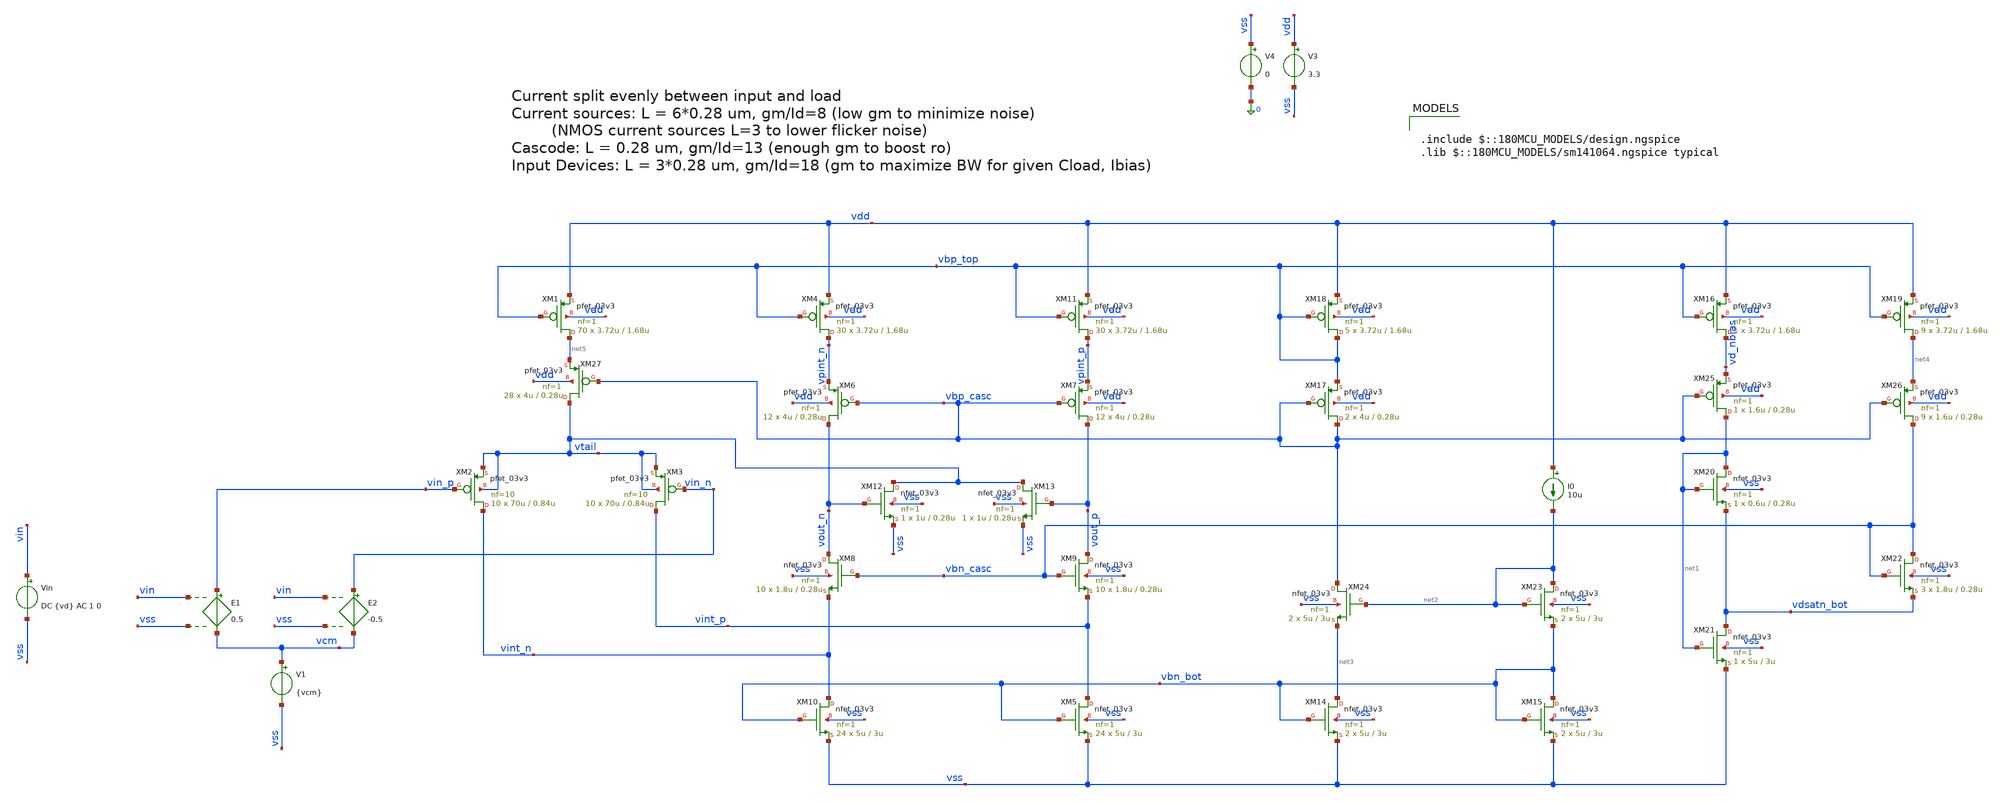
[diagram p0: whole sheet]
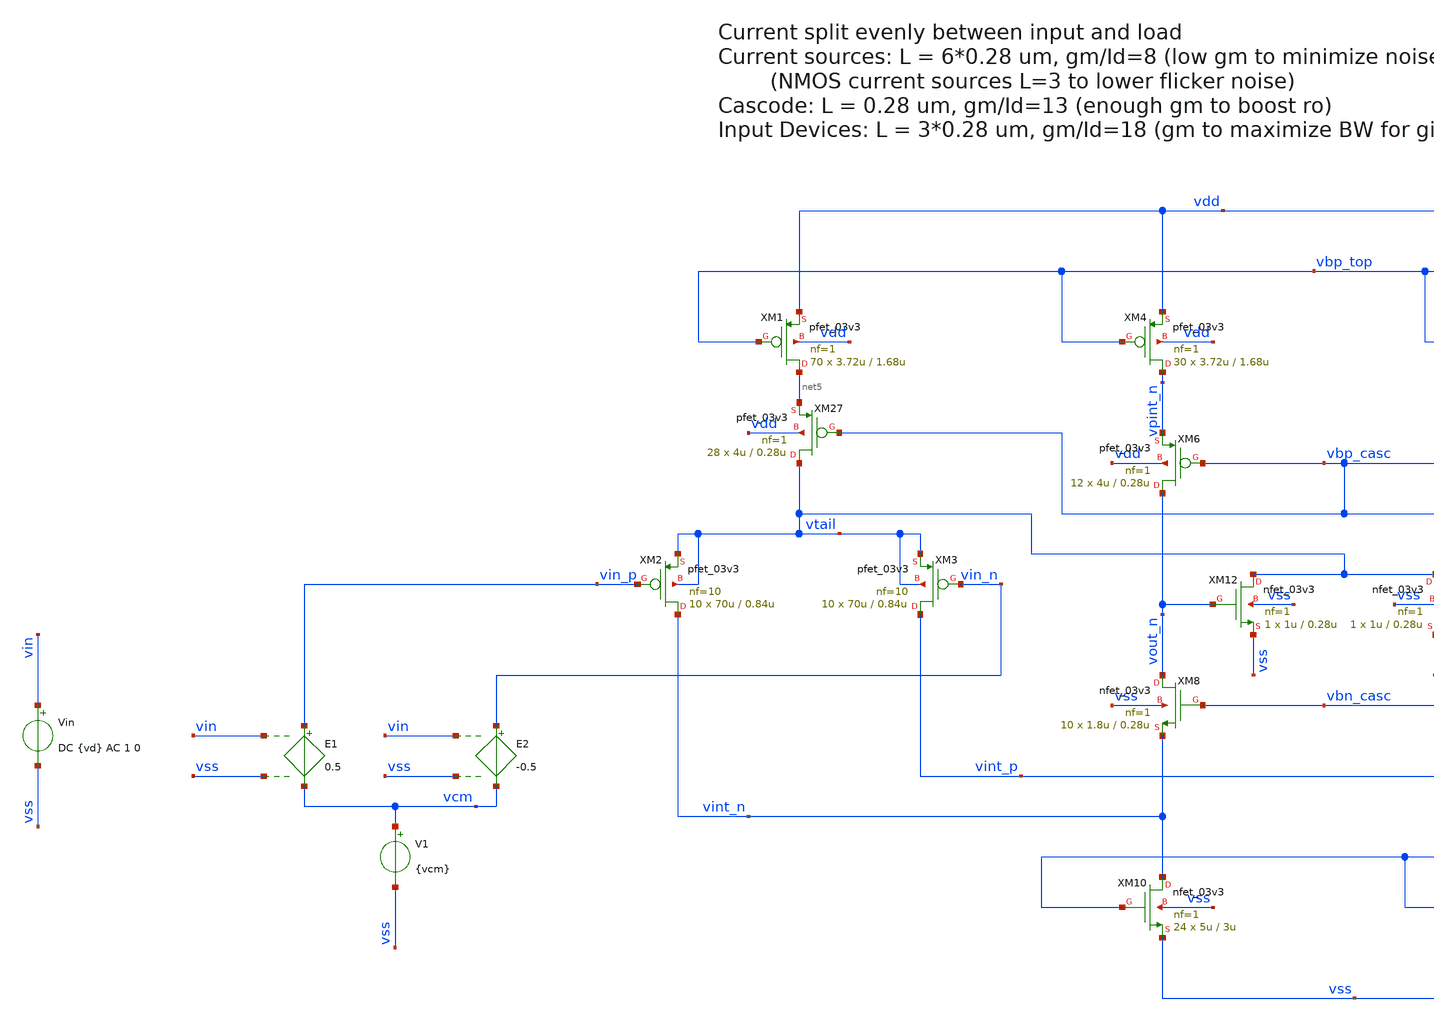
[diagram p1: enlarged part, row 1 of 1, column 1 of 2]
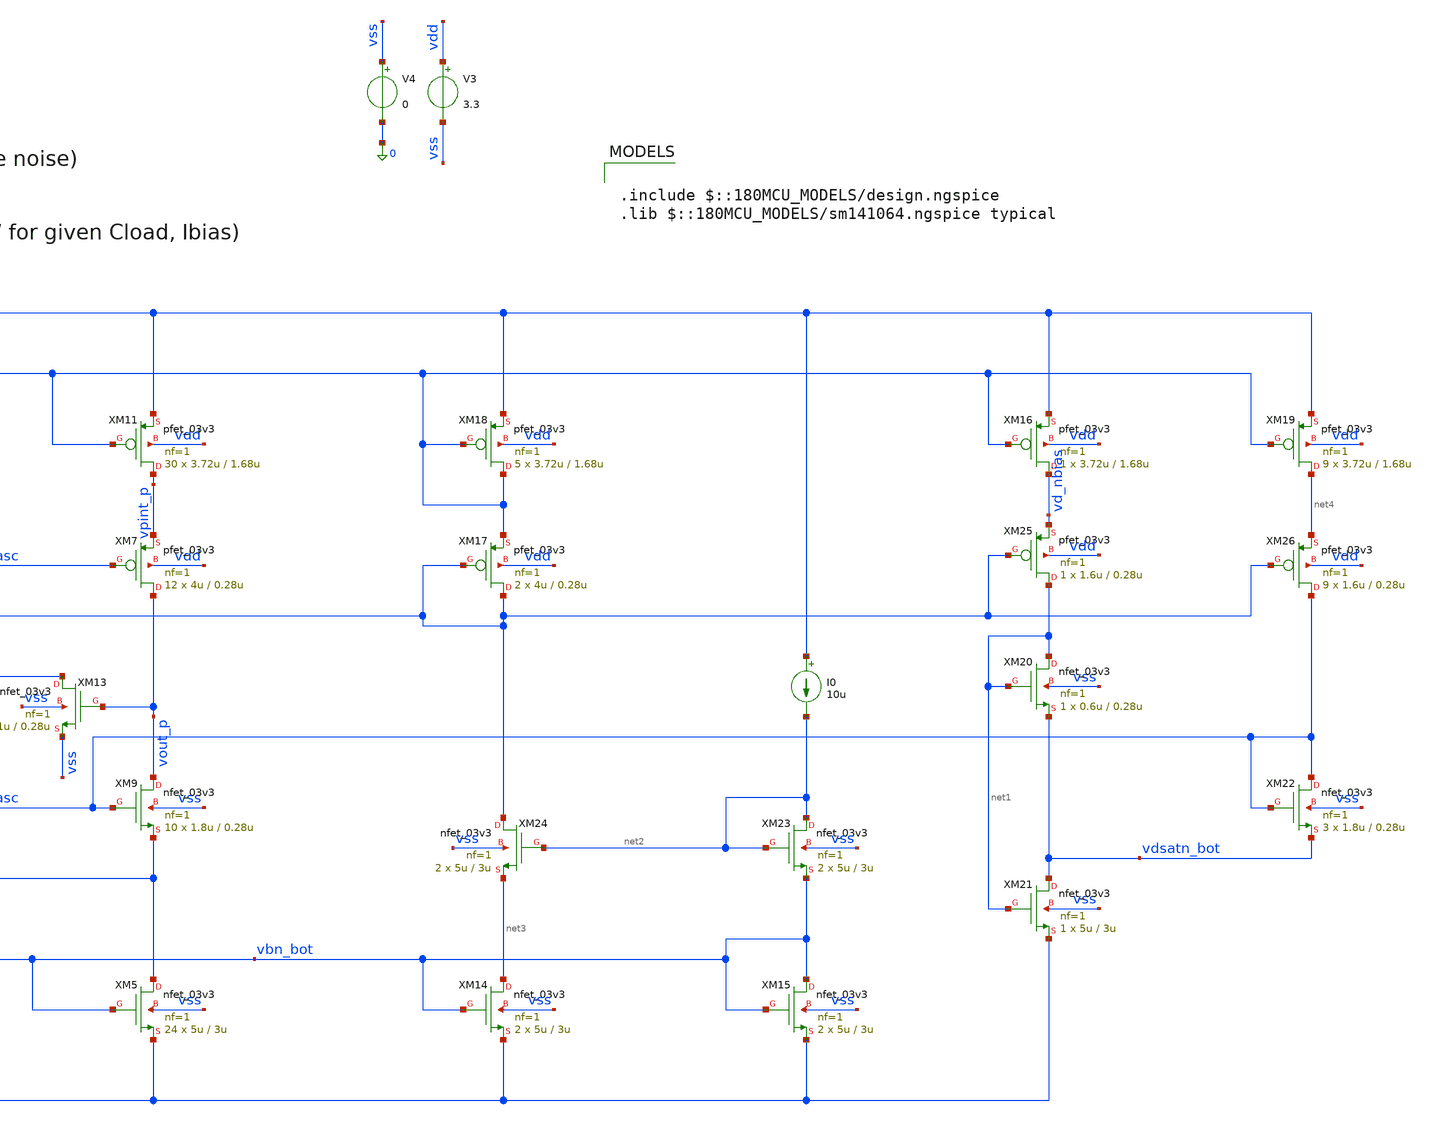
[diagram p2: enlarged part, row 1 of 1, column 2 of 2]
** sch_path: xschem/archive/ota/folded_cascode_test.sch
**.subckt folded_cascode_test
XM2 vint_n vin_p vtail vtail pfet_03v3 L=0.84u W=70u nf=10 ad='int((nf+1)/2) * W/nf * 0.18u' as='int((nf+2)/2) * W/nf * 0.18u'
+ pd='2*int((nf+1)/2) * (W/nf + 0.18u)' ps='2*int((nf+2)/2) * (W/nf + 0.18u)' nrd='0.18u / W' nrs='0.18u / W'
+ sa=0 sb=0 sd=0 m=10
XM1 net5 vbp_top vdd vdd pfet_03v3 L=1.68u W=3.72u nf=1 ad='int((nf+1)/2) * W/nf * 0.18u' as='int((nf+2)/2) * W/nf * 0.18u'
+ pd='2*int((nf+1)/2) * (W/nf + 0.18u)' ps='2*int((nf+2)/2) * (W/nf + 0.18u)' nrd='0.18u / W' nrs='0.18u / W'
+ sa=0 sb=0 sd=0 m=70
XM12 vtail vout_n vss vss nfet_03v3 L=0.28u W=1u nf=1 ad='int((nf+1)/2) * W/nf * 0.18u' as='int((nf+2)/2) * W/nf * 0.18u'
+ pd='2*int((nf+1)/2) * (W/nf + 0.18u)' ps='2*int((nf+2)/2) * (W/nf + 0.18u)' nrd='0.18u / W' nrs='0.18u / W'
+ sa=0 sb=0 sd=0 m=1
XM9 vout_p vbn_casc vint_p vss nfet_03v3 L=0.28u W=1.8u nf=1 ad='int((nf+1)/2) * W/nf * 0.18u' as='int((nf+2)/2) * W/nf * 0.18u'
+ pd='2*int((nf+1)/2) * (W/nf + 0.18u)' ps='2*int((nf+2)/2) * (W/nf + 0.18u)' nrd='0.18u / W' nrs='0.18u / W'
+ sa=0 sb=0 sd=0 m=10
XM7 vout_p vbp_casc vpint_p vdd pfet_03v3 L=0.28u W=4u nf=1 ad='int((nf+1)/2) * W/nf * 0.18u' as='int((nf+2)/2) * W/nf * 0.18u'
+ pd='2*int((nf+1)/2) * (W/nf + 0.18u)' ps='2*int((nf+2)/2) * (W/nf + 0.18u)' nrd='0.18u / W' nrs='0.18u / W'
+ sa=0 sb=0 sd=0 m=12
XM14 net3 vbn_bot vss vss nfet_03v3 L=3u W=5u nf=1 ad='int((nf+1)/2) * W/nf * 0.18u' as='int((nf+2)/2) * W/nf * 0.18u'
+ pd='2*int((nf+1)/2) * (W/nf + 0.18u)' ps='2*int((nf+2)/2) * (W/nf + 0.18u)' nrd='0.18u / W' nrs='0.18u / W'
+ sa=0 sb=0 sd=0 m=2
XM15 vbn_bot vbn_bot vss vss nfet_03v3 L=3u W=5u nf=1 ad='int((nf+1)/2) * W/nf * 0.18u' as='int((nf+2)/2) * W/nf * 0.18u'
+ pd='2*int((nf+1)/2) * (W/nf + 0.18u)' ps='2*int((nf+2)/2) * (W/nf + 0.18u)' nrd='0.18u / W' nrs='0.18u / W'
+ sa=0 sb=0 sd=0 m=2
I0 vdd net2 10u
XM17 vbp_casc vbp_casc vbp_top vdd pfet_03v3 L=0.28u W=4u nf=1 ad='int((nf+1)/2) * W/nf * 0.18u' as='int((nf+2)/2) * W/nf * 0.18u'
+ pd='2*int((nf+1)/2) * (W/nf + 0.18u)' ps='2*int((nf+2)/2) * (W/nf + 0.18u)' nrd='0.18u / W' nrs='0.18u / W'
+ sa=0 sb=0 sd=0 m=2
XM18 vbp_top vbp_top vdd vdd pfet_03v3 L=1.68u W=3.72u nf=1 ad='int((nf+1)/2) * W/nf * 0.18u' as='int((nf+2)/2) * W/nf * 0.18u'
+ pd='2*int((nf+1)/2) * (W/nf + 0.18u)' ps='2*int((nf+2)/2) * (W/nf + 0.18u)' nrd='0.18u / W' nrs='0.18u / W'
+ sa=0 sb=0 sd=0 m=5
V3 vdd vss 3.3
V4 vss 0 0
V1 vcm vss {vcm}
XM3 vint_p vin_n vtail vtail pfet_03v3 L=0.84u W=70u nf=10 ad='int((nf+1)/2) * W/nf * 0.18u' as='int((nf+2)/2) * W/nf * 0.18u'
+ pd='2*int((nf+1)/2) * (W/nf + 0.18u)' ps='2*int((nf+2)/2) * (W/nf + 0.18u)' nrd='0.18u / W' nrs='0.18u / W'
+ sa=0 sb=0 sd=0 m=10
XM4 vpint_n vbp_top vdd vdd pfet_03v3 L=1.68u W=3.72u nf=1 ad='int((nf+1)/2) * W/nf * 0.18u' as='int((nf+2)/2) * W/nf * 0.18u'
+ pd='2*int((nf+1)/2) * (W/nf + 0.18u)' ps='2*int((nf+2)/2) * (W/nf + 0.18u)' nrd='0.18u / W' nrs='0.18u / W'
+ sa=0 sb=0 sd=0 m=30
XM10 vint_n vbn_bot vss vss nfet_03v3 L=3u W=5u nf=1 ad='int((nf+1)/2) * W/nf * 0.18u' as='int((nf+2)/2) * W/nf * 0.18u'
+ pd='2*int((nf+1)/2) * (W/nf + 0.18u)' ps='2*int((nf+2)/2) * (W/nf + 0.18u)' nrd='0.18u / W' nrs='0.18u / W'
+ sa=0 sb=0 sd=0 m=24
XM13 vtail vout_p vss vss nfet_03v3 L=0.28u W=1u nf=1 ad='int((nf+1)/2) * W/nf * 0.18u' as='int((nf+2)/2) * W/nf * 0.18u'
+ pd='2*int((nf+1)/2) * (W/nf + 0.18u)' ps='2*int((nf+2)/2) * (W/nf + 0.18u)' nrd='0.18u / W' nrs='0.18u / W'
+ sa=0 sb=0 sd=0 m=1
XM16 vd_nbias vbp_top vdd vdd pfet_03v3 L=1.68u W=3.72u nf=1 ad='int((nf+1)/2) * W/nf * 0.18u' as='int((nf+2)/2) * W/nf * 0.18u'
+ pd='2*int((nf+1)/2) * (W/nf + 0.18u)' ps='2*int((nf+2)/2) * (W/nf + 0.18u)' nrd='0.18u / W' nrs='0.18u / W'
+ sa=0 sb=0 sd=0 m=1
XM19 net4 vbp_top vdd vdd pfet_03v3 L=1.68u W=3.72u nf=1 ad='int((nf+1)/2) * W/nf * 0.18u' as='int((nf+2)/2) * W/nf * 0.18u'
+ pd='2*int((nf+1)/2) * (W/nf + 0.18u)' ps='2*int((nf+2)/2) * (W/nf + 0.18u)' nrd='0.18u / W' nrs='0.18u / W'
+ sa=0 sb=0 sd=0 m=9
XM22 vbn_casc vbn_casc vdsatn_bot vss nfet_03v3 L=0.28u W=1.8u nf=1 ad='int((nf+1)/2) * W/nf * 0.18u'
+ as='int((nf+2)/2) * W/nf * 0.18u' pd='2*int((nf+1)/2) * (W/nf + 0.18u)' ps='2*int((nf+2)/2) * (W/nf + 0.18u)'
+ nrd='0.18u / W' nrs='0.18u / W' sa=0 sb=0 sd=0 m=3
XM21 vdsatn_bot net1 vss vss nfet_03v3 L=3u W=5u nf=1 ad='int((nf+1)/2) * W/nf * 0.18u' as='int((nf+2)/2) * W/nf * 0.18u'
+ pd='2*int((nf+1)/2) * (W/nf + 0.18u)' ps='2*int((nf+2)/2) * (W/nf + 0.18u)' nrd='0.18u / W' nrs='0.18u / W'
+ sa=0 sb=0 sd=0 m=1
XM8 vout_n vbn_casc vint_n vss nfet_03v3 L=0.28u W=1.8u nf=1 ad='int((nf+1)/2) * W/nf * 0.18u' as='int((nf+2)/2) * W/nf * 0.18u'
+ pd='2*int((nf+1)/2) * (W/nf + 0.18u)' ps='2*int((nf+2)/2) * (W/nf + 0.18u)' nrd='0.18u / W' nrs='0.18u / W'
+ sa=0 sb=0 sd=0 m=10
XM20 net1 net1 vdsatn_bot vss nfet_03v3 L=0.28u W=0.6u nf=1 ad='int((nf+1)/2) * W/nf * 0.18u' as='int((nf+2)/2) * W/nf * 0.18u'
+ pd='2*int((nf+1)/2) * (W/nf + 0.18u)' ps='2*int((nf+2)/2) * (W/nf + 0.18u)' nrd='0.18u / W' nrs='0.18u / W'
+ sa=0 sb=0 sd=0 m=1
E1 vin_p vcm vin vss 0.5
E2 vin_n vcm vin vss -0.5
Vin vin vss DC {vd} AC 1 0
XM5 vint_p vbn_bot vss vss nfet_03v3 L=3u W=5u nf=1 ad='int((nf+1)/2) * W/nf * 0.18u' as='int((nf+2)/2) * W/nf * 0.18u'
+ pd='2*int((nf+1)/2) * (W/nf + 0.18u)' ps='2*int((nf+2)/2) * (W/nf + 0.18u)' nrd='0.18u / W' nrs='0.18u / W'
+ sa=0 sb=0 sd=0 m=24
XM11 vpint_p vbp_top vdd vdd pfet_03v3 L=1.68u W=3.72u nf=1 ad='int((nf+1)/2) * W/nf * 0.18u' as='int((nf+2)/2) * W/nf * 0.18u'
+ pd='2*int((nf+1)/2) * (W/nf + 0.18u)' ps='2*int((nf+2)/2) * (W/nf + 0.18u)' nrd='0.18u / W' nrs='0.18u / W'
+ sa=0 sb=0 sd=0 m=30
XM6 vout_n vbp_casc vpint_n vdd pfet_03v3 L=0.28u W=4u nf=1 ad='int((nf+1)/2) * W/nf * 0.18u' as='int((nf+2)/2) * W/nf * 0.18u'
+ pd='2*int((nf+1)/2) * (W/nf + 0.18u)' ps='2*int((nf+2)/2) * (W/nf + 0.18u)' nrd='0.18u / W' nrs='0.18u / W'
+ sa=0 sb=0 sd=0 m=12
XM23 net2 net2 vbn_bot vss nfet_03v3 L=3u W=5u nf=1 ad='int((nf+1)/2) * W/nf * 0.18u' as='int((nf+2)/2) * W/nf * 0.18u'
+ pd='2*int((nf+1)/2) * (W/nf + 0.18u)' ps='2*int((nf+2)/2) * (W/nf + 0.18u)' nrd='0.18u / W' nrs='0.18u / W'
+ sa=0 sb=0 sd=0 m=2
XM24 vbp_casc net2 net3 vss nfet_03v3 L=3u W=5u nf=1 ad='int((nf+1)/2) * W/nf * 0.18u' as='int((nf+2)/2) * W/nf * 0.18u'
+ pd='2*int((nf+1)/2) * (W/nf + 0.18u)' ps='2*int((nf+2)/2) * (W/nf + 0.18u)' nrd='0.18u / W' nrs='0.18u / W'
+ sa=0 sb=0 sd=0 m=2
XM25 net1 vbp_casc vd_nbias vdd pfet_03v3 L=0.28u W=1.6u nf=1 ad='int((nf+1)/2) * W/nf * 0.18u' as='int((nf+2)/2) * W/nf * 0.18u'
+ pd='2*int((nf+1)/2) * (W/nf + 0.18u)' ps='2*int((nf+2)/2) * (W/nf + 0.18u)' nrd='0.18u / W' nrs='0.18u / W'
+ sa=0 sb=0 sd=0 m=1
XM26 vbn_casc vbp_casc net4 vdd pfet_03v3 L=0.28u W=1.6u nf=1 ad='int((nf+1)/2) * W/nf * 0.18u' as='int((nf+2)/2) * W/nf * 0.18u'
+ pd='2*int((nf+1)/2) * (W/nf + 0.18u)' ps='2*int((nf+2)/2) * (W/nf + 0.18u)' nrd='0.18u / W' nrs='0.18u / W'
+ sa=0 sb=0 sd=0 m=9
XM27 vtail vbp_casc net5 vdd pfet_03v3 L=0.28u W=4u nf=1 ad='int((nf+1)/2) * W/nf * 0.18u' as='int((nf+2)/2) * W/nf * 0.18u'
+ pd='2*int((nf+1)/2) * (W/nf + 0.18u)' ps='2*int((nf+2)/2) * (W/nf + 0.18u)' nrd='0.18u / W' nrs='0.18u / W'
+ sa=0 sb=0 sd=0 m=28
**** begin user architecture code

.param vcm=0.5
.param vd=0
.control
save all
save @m.x1.x1.xm2.m0[id] @m.x1.x1.xm2.m0[gm] @m.x1.x1.xm2.m0[gds]
save @m.x1.x1.xm1.m0[id] @m.x1.x1.xm1.m0[gm] @m.x1.x1.xm1.m0[gds]
save @m.x1.x2.xm1.m0[id] @m.x1.x2.xm1.m0[gm] @m.x1.x2.xm1.m0[gds]
save @m.x1.x2.xm7.m0[id] @m.x1.x2.xm7.m0[gm] @m.x1.x2.xm7.m0[gds]
save @m.x1.x2.xm17.m0[id] @m.x1.x2.xm17.m0[gm] @m.x1.x2.xm17.m0[gds]
save @m.x1.x2.xm18.m0[id] @m.x1.x2.xm18.m0[gm] @m.x1.x2.xm18.m0[gds]
save @m.x1.x2.xm4.m0[id] @m.x1.x2.xm4.m0[gm] @m.x1.x2.xm4.m0[gds]
save @m.x1.x2.xm16.m0[id] @m.x1.x2.xm16.m0[gm] @m.x1.x2.xm16.m0[gds]
save @m.x1.x2.xm19.m0[id] @m.x1.x2.xm19.m0[gm] @m.x1.x2.xm19.m0[gds]
save @m.x1.x2.xm11.m0[id] @m.x1.x2.xm11.m0[gm] @m.x1.x2.xm11.m0[gds]
save @m.x1.x2.xm6.m0[id] @m.x1.x2.xm6.m0[gm] @m.x1.x2.xm6.m0[gds]
save @m.x1.x2.xm25.m0[id] @m.x1.x2.xm25.m0[gm] @m.x1.x2.xm25.m0[gds]
save @m.x1.x2.xm26.m0[id] @m.x1.x2.xm26.m0[gm] @m.x1.x2.xm26.m0[gds]
save @m.x1.x2.xm27.m0[id] @m.x1.x2.xm27.m0[gm] @m.x1.x2.xm27.m0[gds]
save @m.x1.x3.xm14.m0[id] @m.x1.x3.xm14.m0[gm] @m.x1.x3.xm14.m0[gds]
save @m.x1.x3.xm15.m0[id] @m.x1.x3.xm15.m0[gm] @m.x1.x3.xm15.m0[gds]
save @m.x1.x3.xm10.m0[id] @m.x1.x3.xm10.m0[gm] @m.x1.x3.xm10.m0[gds]
save @m.x1.x3.xm5.m0[id] @m.x1.x3.xm5.m0[gm] @m.x1.x3.xm5.m0[gds]
save @m.x1.x3.xm23.m0[id] @m.x1.x3.xm23.m0[gm] @m.x1.x3.xm23.m0[gds]
save @m.x1.x3.xm24.m0[id] @m.x1.x3.xm24.m0[gm] @m.x1.x3.xm24.m0[gds]
save @m.x1.x4.xm9.m0[id] @m.x1.x4.xm9.m0[gm] @m.x1.x4.xm9.m0[gds]
save @m.x1.x4.xm22.m0[id] @m.x1.x4.xm22.m0[gm] @m.x1.x4.xm22.m0[gds]
save @m.x1.x4.xm21.m0[id] @m.x1.x4.xm21.m0[gm] @m.x1.x4.xm21.m0[gds]
save @m.x1.x4.xm8.m0[id] @m.x1.x4.xm8.m0[gm] @m.x1.x4.xm8.m0[gds]
save @m.x1.x4.xm20.m0[id] @m.x1.x4.xm20.m0[gm] @m.x1.x4.xm20.m0[gds]
save @m.x1.x5.xm1.m0[id] @m.x1.x5.xm1.m0[gm] @m.x1.x5.xm1.m0[gds]
save @m.x1.x5.xm2.m0[id] @m.x1.x5.xm2.m0[gm] @m.x1.x5.xm2.m0[gds]
save @m.x1.x6.xm15.m0[id] @m.x1.x6.xm15.m0[gm] @m.x1.x6.xm15.m0[gds]
save @m.x1.x6.xm1.m0[id] @m.x1.x6.xm1.m0[gm] @m.x1.x6.xm1.m0[gds]
save @m.x1.x6.xm2.m0[id] @m.x1.x6.xm2.m0[gm] @m.x1.x6.xm2.m0[gds]
save @m.x1.x6.xm3.m0[id] @m.x1.x6.xm3.m0[gm] @m.x1.x6.xm3.m0[gds]
save @m.x1.x6.xm7.m0[id] @m.x1.x6.xm7.m0[gm] @m.x1.x6.xm7.m0[gds]
save @m.x1.x6.xm8.m0[id] @m.x1.x6.xm8.m0[gm] @m.x1.x6.xm8.m0[gds]
save @m.x1.x6.xm4.m0[id] @m.x1.x6.xm4.m0[gm] @m.x1.x6.xm4.m0[gds]
save @m.x1.x6.xm5.m0[id] @m.x1.x6.xm5.m0[gm] @m.x1.x6.xm5.m0[gds]
save @m.x1.x6.xm6.m0[id] @m.x1.x6.xm6.m0[gm] @m.x1.x6.xm6.m0[gds]
save @m.x1.x7.xm6.m0[id] @m.x1.x7.xm6.m0[gm] @m.x1.x7.xm6.m0[gds]
save @m.x1.x7.xm5.m0[id] @m.x1.x7.xm5.m0[gm] @m.x1.x7.xm5.m0[gds]
save @m.x1.x7.xm1.m0[id] @m.x1.x7.xm1.m0[gm] @m.x1.x7.xm1.m0[gds]
save @m.x1.x7.xm2.m0[id] @m.x1.x7.xm2.m0[gm] @m.x1.x7.xm2.m0[gds]
save @m.x1.x7.xm3.m0[id] @m.x1.x7.xm3.m0[gm] @m.x1.x7.xm3.m0[gds]
save @m.x1.x7.xm4.m0[id] @m.x1.x7.xm4.m0[gm] @m.x1.x7.xm4.m0[gds]
save @m.x1.x8.xm6.m0[id] @m.x1.x8.xm6.m0[gm] @m.x1.x8.xm6.m0[gds]
save @m.x1.x8.xm5.m0[id] @m.x1.x8.xm5.m0[gm] @m.x1.x8.xm5.m0[gds]
save @m.x1.x8.xm1.m0[id] @m.x1.x8.xm1.m0[gm] @m.x1.x8.xm1.m0[gds]
save @m.x1.x8.xm2.m0[id] @m.x1.x8.xm2.m0[gm] @m.x1.x8.xm2.m0[gds]
save @m.x1.x8.xm3.m0[id] @m.x1.x8.xm3.m0[gm] @m.x1.x8.xm3.m0[gds]
save @m.x1.x8.xm4.m0[id] @m.x1.x8.xm4.m0[gm] @m.x1.x8.xm4.m0[gds]
op
write results_op.raw all
noise v(vout_p, vout_n) Vin dec 10 1 1000Meg
ac dec 100 1 10G
.endc


.include $::180MCU_MODELS/design.ngspice
.lib $::180MCU_MODELS/sm141064.ngspice typical

**** end user architecture code
**.ends
.end
